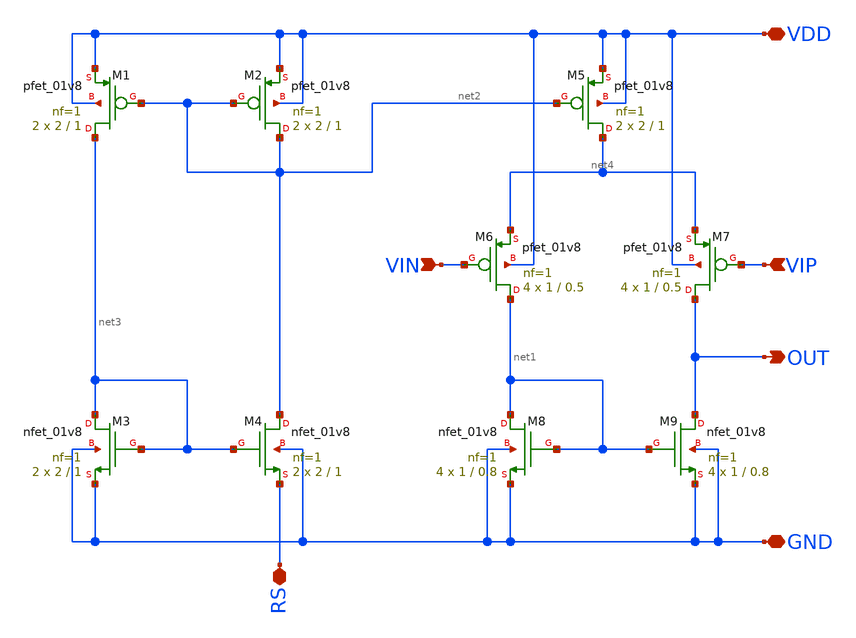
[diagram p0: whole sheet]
** sch_path: opamp/xschem/opamp.sch
**.subckt opamp VDD GND RS VIN VIP OUT
*.iopin VDD
*.iopin GND
*.iopin RS
*.ipin VIN
*.ipin VIP
*.opin OUT
XM1 net3 net2 VDD VDD sky130_fd_pr__pfet_01v8 L=1 W=2 nf=1 ad='int((nf+1)/2) * W/nf * 0.29' as='int((nf+2)/2) * W/nf * 0.29'
+ pd='2*int((nf+1)/2) * (W/nf + 0.29)' ps='2*int((nf+2)/2) * (W/nf + 0.29)' nrd='0.29 / W' nrs='0.29 / W'
+ sa=0 sb=0 sd=0 mult=2 m=2
XM2 net2 net2 VDD VDD sky130_fd_pr__pfet_01v8 L=1 W=2 nf=1 ad='int((nf+1)/2) * W/nf * 0.29' as='int((nf+2)/2) * W/nf * 0.29'
+ pd='2*int((nf+1)/2) * (W/nf + 0.29)' ps='2*int((nf+2)/2) * (W/nf + 0.29)' nrd='0.29 / W' nrs='0.29 / W'
+ sa=0 sb=0 sd=0 mult=2 m=2
XM3 net3 net3 GND GND sky130_fd_pr__nfet_01v8 L=1 W=2 nf=1 ad='int((nf+1)/2) * W/nf * 0.29' as='int((nf+2)/2) * W/nf * 0.29'
+ pd='2*int((nf+1)/2) * (W/nf + 0.29)' ps='2*int((nf+2)/2) * (W/nf + 0.29)' nrd='0.29 / W' nrs='0.29 / W'
+ sa=0 sb=0 sd=0 mult=2 m=2
XM4 net2 net3 RS GND sky130_fd_pr__nfet_01v8 L=1 W=2 nf=1 ad='int((nf+1)/2) * W/nf * 0.29' as='int((nf+2)/2) * W/nf * 0.29'
+ pd='2*int((nf+1)/2) * (W/nf + 0.29)' ps='2*int((nf+2)/2) * (W/nf + 0.29)' nrd='0.29 / W' nrs='0.29 / W'
+ sa=0 sb=0 sd=0 mult=2 m=2
XM5 net4 net2 VDD VDD sky130_fd_pr__pfet_01v8 L=1 W=2 nf=1 ad='int((nf+1)/2) * W/nf * 0.29' as='int((nf+2)/2) * W/nf * 0.29'
+ pd='2*int((nf+1)/2) * (W/nf + 0.29)' ps='2*int((nf+2)/2) * (W/nf + 0.29)' nrd='0.29 / W' nrs='0.29 / W'
+ sa=0 sb=0 sd=0 mult=2 m=2
XM6 net1 VIN net4 VDD sky130_fd_pr__pfet_01v8 L=0.5 W=1 nf=1 ad='int((nf+1)/2) * W/nf * 0.29' as='int((nf+2)/2) * W/nf * 0.29'
+ pd='2*int((nf+1)/2) * (W/nf + 0.29)' ps='2*int((nf+2)/2) * (W/nf + 0.29)' nrd='0.29 / W' nrs='0.29 / W'
+ sa=0 sb=0 sd=0 mult=4 m=4
XM7 OUT VIP net4 VDD sky130_fd_pr__pfet_01v8 L=0.5 W=1 nf=1 ad='int((nf+1)/2) * W/nf * 0.29' as='int((nf+2)/2) * W/nf * 0.29'
+ pd='2*int((nf+1)/2) * (W/nf + 0.29)' ps='2*int((nf+2)/2) * (W/nf + 0.29)' nrd='0.29 / W' nrs='0.29 / W'
+ sa=0 sb=0 sd=0 mult=4 m=4
XM8 net1 net1 GND GND sky130_fd_pr__nfet_01v8 L=0.8 W=1 nf=1 ad='int((nf+1)/2) * W/nf * 0.29' as='int((nf+2)/2) * W/nf * 0.29'
+ pd='2*int((nf+1)/2) * (W/nf + 0.29)' ps='2*int((nf+2)/2) * (W/nf + 0.29)' nrd='0.29 / W' nrs='0.29 / W'
+ sa=0 sb=0 sd=0 mult=4 m=4
XM9 OUT net1 GND GND sky130_fd_pr__nfet_01v8 L=0.8 W=1 nf=1 ad='int((nf+1)/2) * W/nf * 0.29' as='int((nf+2)/2) * W/nf * 0.29'
+ pd='2*int((nf+1)/2) * (W/nf + 0.29)' ps='2*int((nf+2)/2) * (W/nf + 0.29)' nrd='0.29 / W' nrs='0.29 / W'
+ sa=0 sb=0 sd=0 mult=4 m=4
**.ends
.end
